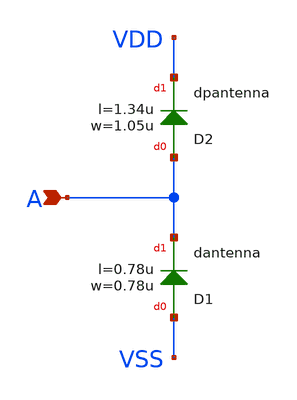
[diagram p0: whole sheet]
** sch_path: ADC8711-main/schematic/xschem/sg13g2_hv_antennanp.sch
**.subckt sg13g2_hv_antennanp A
*.ipin A
XD1 VSS A dantenna l=0.78u w=0.78u
XD2 A VDD dpantenna l=1.34u w=1.05u
**.ends
.end
